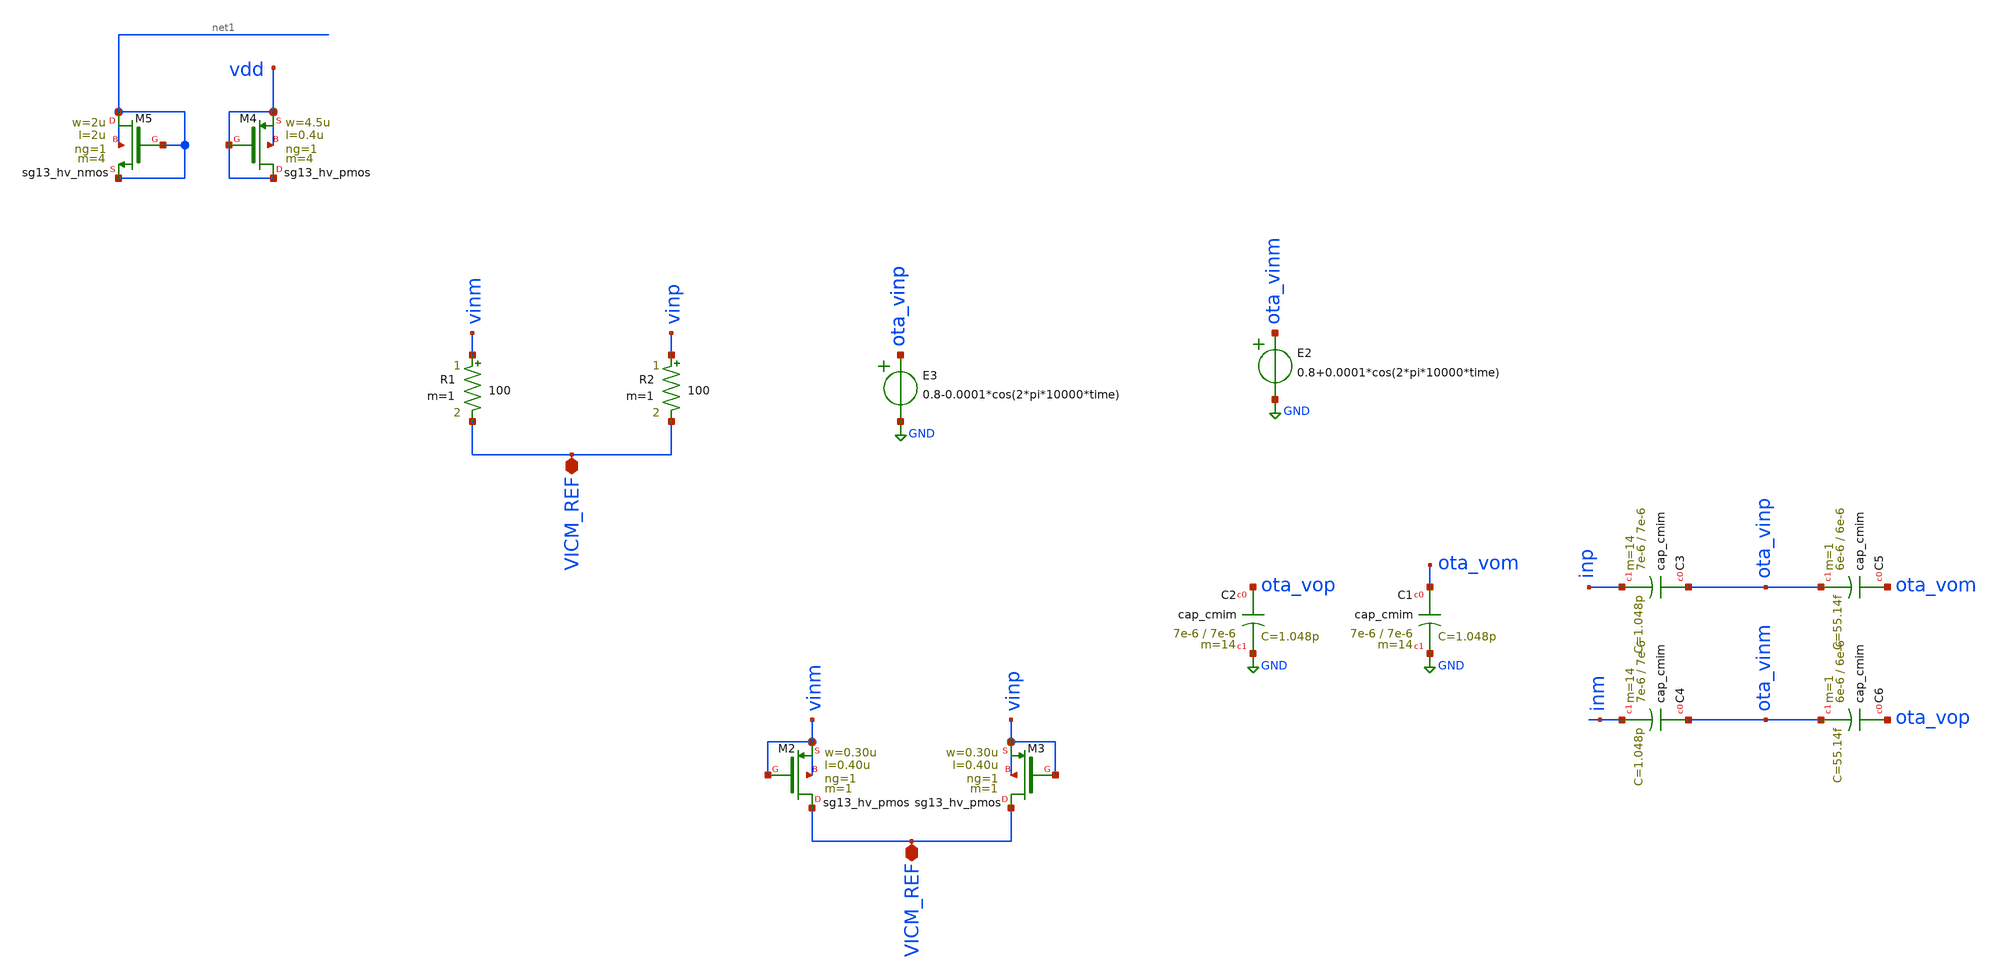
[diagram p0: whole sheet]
** sch_path: temp.sch
**.subckt temp VICM_REF VICM_REF
*.iopin VICM_REF
*.iopin VICM_REF
XC1 ota_vom GND cap_cmim w=7e-6 l=7e-6 m=14 mm_ok=1
XC2 ota_vop GND cap_cmim w=7e-6 l=7e-6 m=14 mm_ok=1
XC3 ota_vinp inp cap_cmim w=7e-6 l=7e-6 m=14 mm_ok=1
XC4 ota_vinm inm cap_cmim w=7e-6 l=7e-6 m=14 mm_ok=1
XC5 ota_vom ota_vinp cap_cmim w=6e-6 l=6e-6 m=1 mm_ok=1
XC6 ota_vop ota_vinm cap_cmim w=6e-6 l=6e-6 m=1 mm_ok=1
E2 ota_vinm GND VOL=' 0.8+0.0001*cos(2*pi*10000*time) '
E3 ota_vinp GND VOL=' 0.8-0.0001*cos(2*pi*10000*time) '
XM2 VICM_REF vinm vinm vinm sg13_hv_pmos w=0.30u l=0.40u ng=1 m=1 mm_ok=1
XM3 VICM_REF vinp vinp vinp sg13_hv_pmos w=0.30u l=0.40u ng=1 m=1 mm_ok=1
R1 vinm VICM_REF 100 m=1
R2 vinp VICM_REF 100 m=1
XM4 vdd vdd vdd vdd sg13_hv_pmos w=4.5u l=0.4u ng=1 m=4 mm_ok=1
XM5 net1 net1 net1 net1 sg13_hv_nmos w=2u l=2u ng=1 m=4 mm_ok=1
**.ends
.GLOBAL GND
.end
